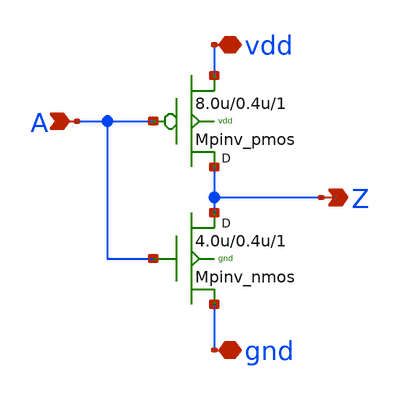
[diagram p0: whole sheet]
** sch_path: sram_4_16_scn4m/pinv_10.sch
**.subckt pinv_10 A Z vdd gnd
*.ipin A
*.opin Z
*.iopin vdd
*.iopin gnd
Mpinv_nmos Z A gnd gnd n w=4.0u l=0.4u m=1
Mpinv_pmos Z A vdd vdd p w=8.0u l=0.4u m=1
**.ends
.end
